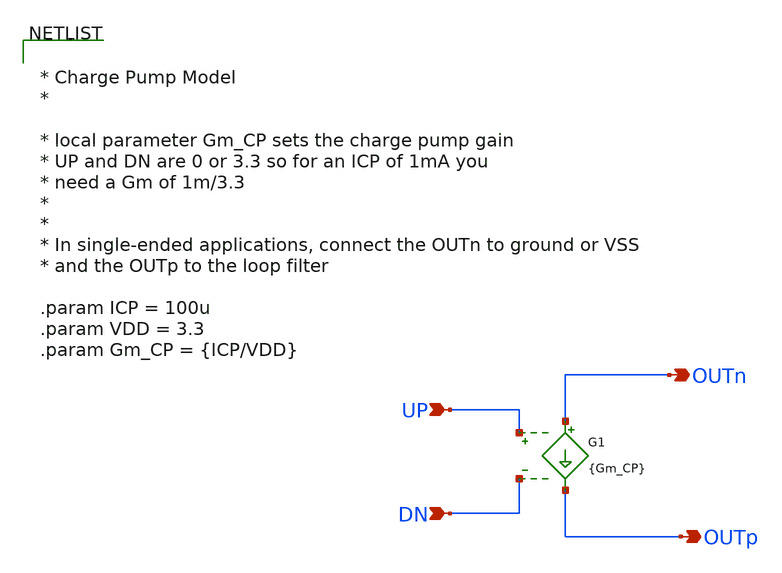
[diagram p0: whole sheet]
** sch_path: designs/libs/model_pll/CP_model.sch
**.subckt CP_model UP DN OUTp OUTn
*.ipin UP
*.ipin DN
*.opin OUTp
*.opin OUTn
G1 OUTn OUTp UP DN {Gm_CP}
**** begin user architecture code


* Charge Pump Model
*

* local parameter Gm_CP sets the charge pump gain
* UP and DN are 0 or 3.3 so for an ICP of 1mA you
* need a Gm of 1m/3.3
*
*
* In single-ended applications, connect the OUTn to ground or VSS
* and the OUTp to the loop filter

.param ICP = 100u
.param VDD = 3.3
.param Gm_CP = {ICP/VDD}



**** end user architecture code
**.ends
.end
